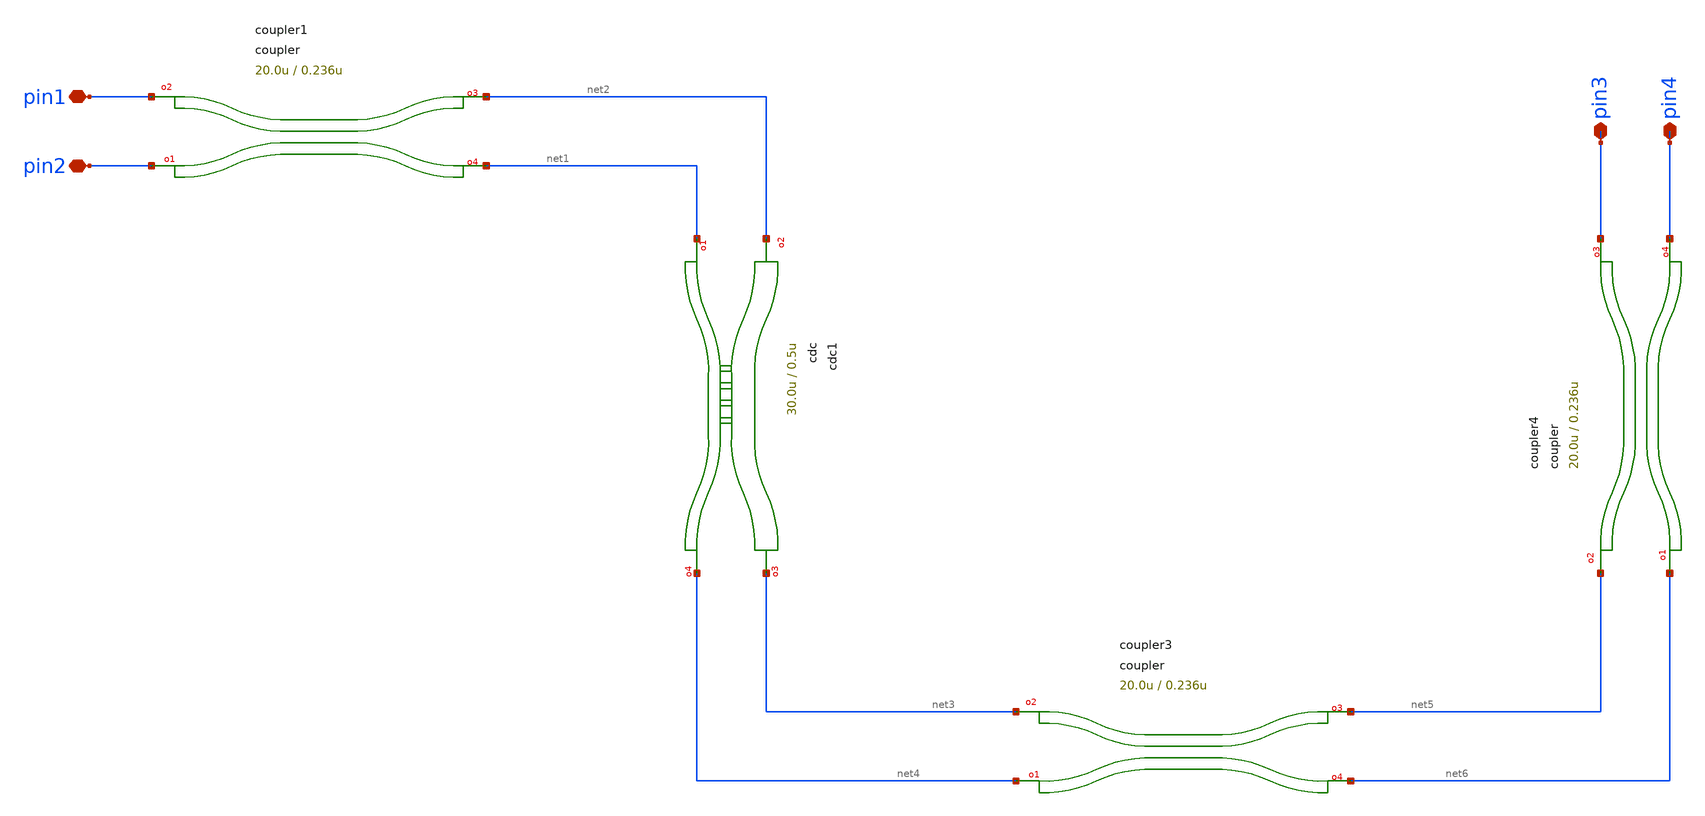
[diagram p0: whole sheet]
** sch_path: xschem/tests/test_sch/test_coupler.sch
* Copyright (c) 2024, Mabrains LLC
* Licensed under the GNU Lesser General Public License, Version 3.0 (the "License");
* you may not use this file except in compliance with the License.
* GNU Lesser General Public License
* Version 3, 29 June 2007
* This program is free software: you can redistribute it and/or modify
* it under the terms of the GNU Lesser General Public License as published
* by the Free Software Foundation, either version 3 of the License, or
* (at your option) any later version.
* This program is distributed in the hope that it will be useful,
* but WITHOUT ANY WARRANTY; without even the implied warranty of
* MERCHANTABILITY or FITNESS FOR A PARTICULAR PURPOSE.  See the
* GNU Lesser General Public License for more details.
* You should have received a copy of the GNU Lesser General Public License
* along with this program.  If not, see <https://www.gnu.org/licenses/>.
* SPDX-License-Identifier: LGPL-3.0
**.subckt test_coupler pin1 pin2 pin3 pin4
*.iopin pin1
*.iopin pin2
*.iopin pin3
*.iopin pin4
Pcoupler1 pin1 pin2 net2 net1 coupler length=20.0u gap=0.236u dx=10u dy=4.0u
Pcoupler3 net3 net4 net5 net6 coupler length=20.0u gap=0.236u dx=10u dy=4.0u
Pcoupler4 net5 net6 pin3 pin4 coupler length=20.0u gap=0.236u dx=10u dy=4.0u
Pcdc1 net2 net1 net3 net4 cdc length=30.0u gap=0.5u period=0.22 duty_cycle=0.5 width_top=2.0u
+ width_bot=0.75u dx=10u dy=1.8u
**.ends
.end
